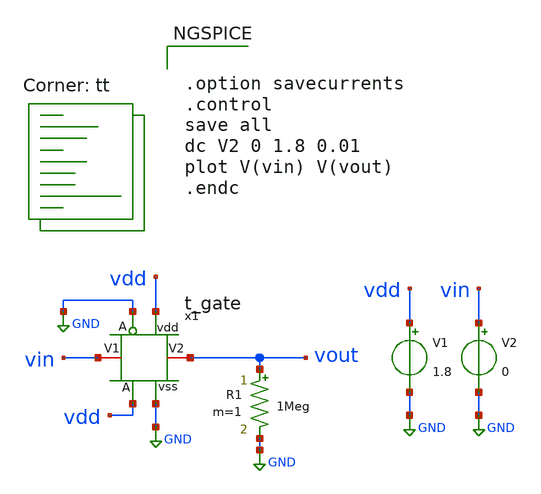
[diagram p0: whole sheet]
** sch_path: xschem/t-gate/t_gate_tb.sch
**.subckt t_gate_tb
V1 vdd GND 1.8
V2 vin GND 0
R1 vout GND 1Meg m=1
x1 GND vdd vin vout GND vdd t_gate
**** begin user architecture code
.lib $::SKYWATER_MODELS/sky130.lib.spice tt


.option savecurrents
.control
save all
dc V2 0 1.8 0.01
plot V(vin) V(vout)
.endc


**** end user architecture code
**.ends

* expanding   symbol:  /foss/designs/dac10b-r2r-sky130/xschem/t-gate/t_gate.sym # of pins=6
** sym_path: xschem/t-gate/t_gate.sym
** sch_path: xschem/t-gate/t_gate.sch
.subckt t_gate A_p vdd V1 V2 vss A_n
*.iopin V1
*.iopin V2
*.ipin A_p
*.ipin vdd
*.ipin vss
*.ipin A_n
XM2 V1 A_n V2 vss sky130_fd_pr__nfet_01v8 L=0.17 W=1 nf=1 ad={int((nf+1)/2) * W/nf * 0.29} as={int((nf+2)/2) * W/nf * 0.29}
+ pd={2*int((nf+1)/2) * (W/nf + 0.29)} ps={2*int((nf+2)/2) * (W/nf + 0.29)} nrd={0.29 / W} nrs={0.29 / W}
+ sa=0 sb=0 sd=0 mult=1 m=1
XM1 V1 A_p V2 vdd sky130_fd_pr__pfet_01v8 L=0.17 W=1 nf=1 ad={int((nf+1)/2) * W/nf * 0.29} as={int((nf+2)/2) * W/nf * 0.29}
+ pd={2*int((nf+1)/2) * (W/nf + 0.29)} ps={2*int((nf+2)/2) * (W/nf + 0.29)} nrd={0.29 / W} nrs={0.29 / W}
+ sa=0 sb=0 sd=0 mult=1 m=1
.ends

.GLOBAL GND
.end
